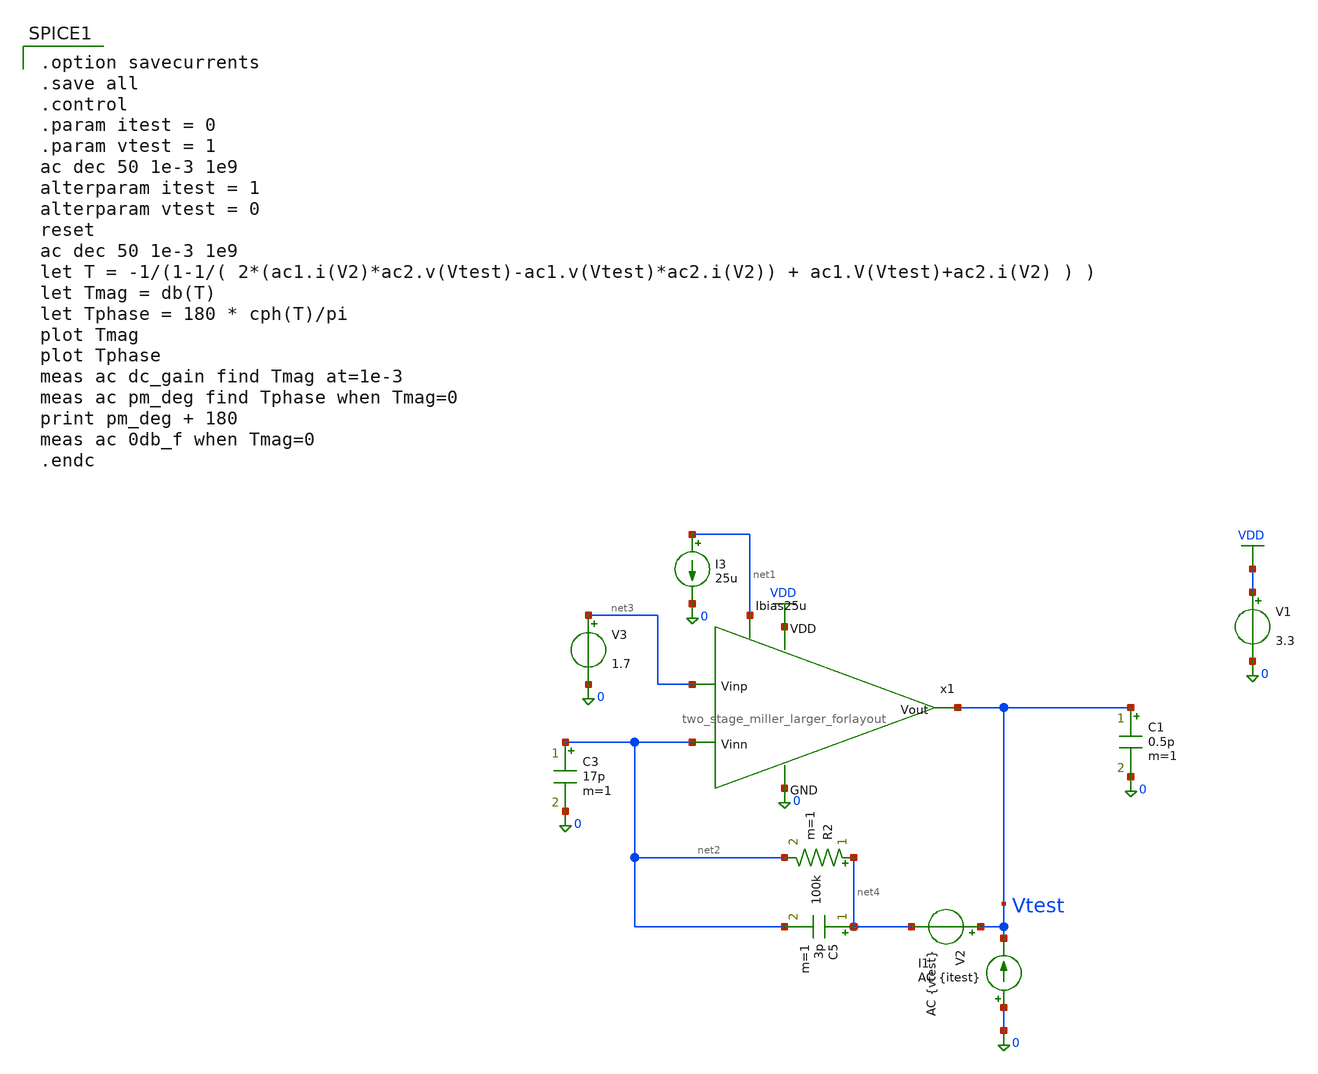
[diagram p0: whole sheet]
** sch_path: jz_tia/xschem/tia_loopgain_tb.sch
**.subckt tia_loopgain_tb
V1 VDD 0 3.3
C3 net2 0 17p m=1
R2 net4 net2 100k m=1
C5 net4 net2 3p m=1
V3 net3 0 1.7
I3 net1 0 25u
V2 Vtest net4 AC {vtest}
I1 0 Vtest AC {itest}
C1 Vtest 0 0.5p m=1
x1 VDD Vtest net3 net2 net1 0 two_stage_miller_larger_forlayout
**** begin user architecture code

.option savecurrents
.save all
.control
.param itest = 0
.param vtest = 1
ac dec 50 1e-3 1e9
alterparam itest = 1
alterparam vtest = 0
reset
ac dec 50 1e-3 1e9
let T = -1/(1-1/( 2*(ac1.i(V2)*ac2.v(Vtest)-ac1.v(Vtest)*ac2.i(V2)) + ac1.V(Vtest)+ac2.i(V2) ) )
let Tmag = db(T)
let Tphase = 180 * cph(T)/pi
plot Tmag
plot Tphase
meas ac dc_gain find Tmag at=1e-3
meas ac pm_deg find Tphase when Tmag=0
print pm_deg + 180
meas ac 0db_f when Tmag=0
.endc


.include $::180MCU_MODELS/design.ngspice
.lib $::180MCU_MODELS/sm141064.ngspice typical
.lib $::180MCU_MODELS/sm141064.ngspice res_typical
.lib $::180MCU_MODELS/sm141064.ngspice cap_mim
.lib $::180MCU_MODELS/sm141064.ngspice mimcap_typical

**** end user architecture code
**.ends
.GLOBAL VDD
.end
